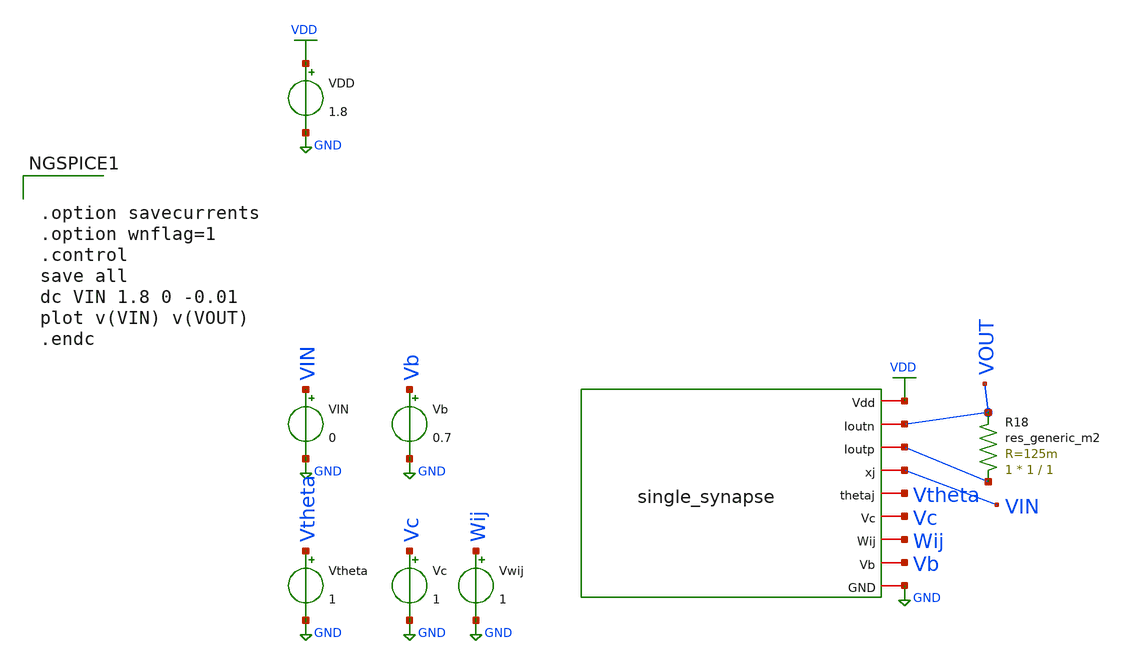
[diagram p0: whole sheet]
** sch_path: test_single_synapse.sch
**.subckt test_single_synapse
x1 VDD VOUT net1 VIN Vtheta Vc Wij Vb GND single_synapse
VDD VDD GND 1.8
VIN VIN GND 0
R18 net1 VOUT sky130_fd_pr__res_generic_m2 W=1 L=1 m=1
Vb Vb GND 0.7
Vtheta Vtheta GND 1
Vc Vc GND 1
Vwij Wij GND 1
**** begin user architecture code


.option savecurrents
.option wnflag=1
.control
save all
dc VIN 1.8 0 -0.01
plot v(VIN) v(VOUT)
.endc



** opencircuitdesign pdks install
.lib $::SKYWATER_MODELS/sky130.lib.spice tt


**** end user architecture code
**.ends
.GLOBAL GND
.GLOBAL VDD
.end
